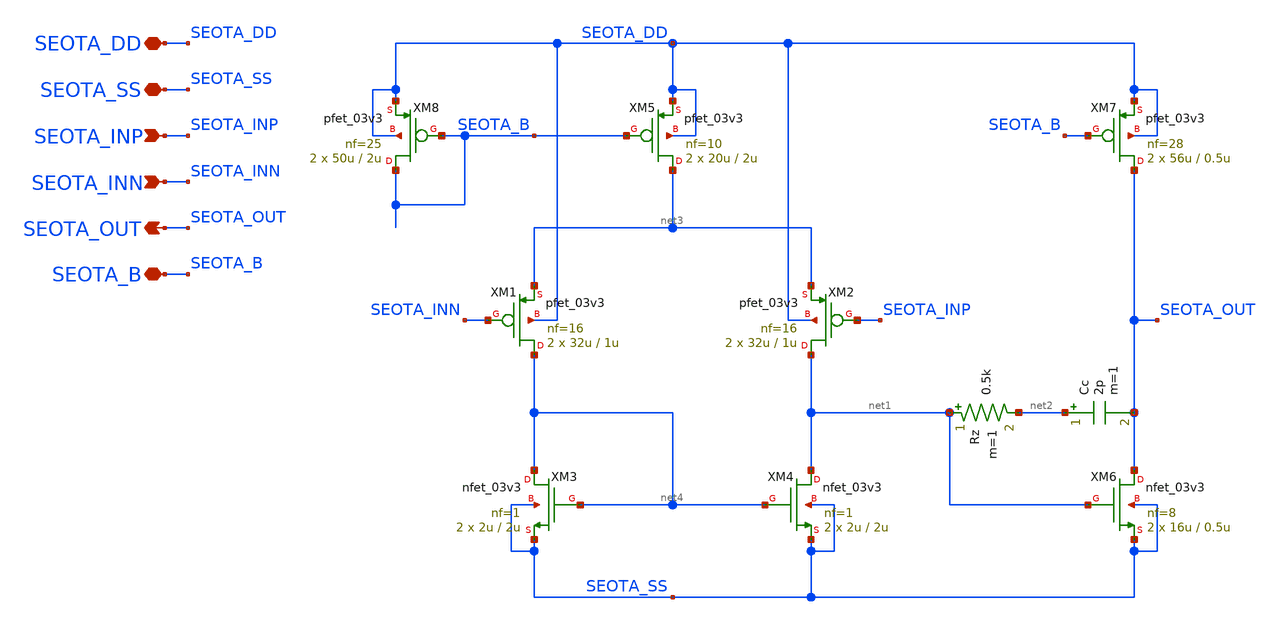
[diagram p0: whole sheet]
** sch_path: Design_Files/IC Design/Schematic/SE_OTA/SE_OTA.sch
**.subckt SE_OTA SEOTA_DD SEOTA_SS SEOTA_INP SEOTA_INN SEOTA_OUT SEOTA_B
*.iopin SEOTA_DD
*.iopin SEOTA_SS
*.ipin SEOTA_INP
*.ipin SEOTA_INN
*.opin SEOTA_OUT
*.iopin SEOTA_B
XM4 net1 net4 SEOTA_SS SEOTA_SS nfet_03v3 L=2u W=2u nf=1 ad='int((nf+1)/2) * W/nf * 0.18u' as='int((nf+2)/2) * W/nf * 0.18u'
+ pd='2*int((nf+1)/2) * (W/nf + 0.18u)' ps='2*int((nf+2)/2) * (W/nf + 0.18u)' nrd='0.18u / W' nrs='0.18u / W'
+ sa=0 sb=0 sd=0 m=2
XM3 net4 net4 SEOTA_SS SEOTA_SS nfet_03v3 L=2u W=2u nf=1 ad='int((nf+1)/2) * W/nf * 0.18u' as='int((nf+2)/2) * W/nf * 0.18u'
+ pd='2*int((nf+1)/2) * (W/nf + 0.18u)' ps='2*int((nf+2)/2) * (W/nf + 0.18u)' nrd='0.18u / W' nrs='0.18u / W'
+ sa=0 sb=0 sd=0 m=2
XM1 net4 SEOTA_INN net3 SEOTA_DD pfet_03v3 L=1u W=32u nf=16 ad='int((nf+1)/2) * W/nf * 0.18u' as='int((nf+2)/2) * W/nf * 0.18u'
+ pd='2*int((nf+1)/2) * (W/nf + 0.18u)' ps='2*int((nf+2)/2) * (W/nf + 0.18u)' nrd='0.18u / W' nrs='0.18u / W'
+ sa=0 sb=0 sd=0 m=2
XM2 net1 SEOTA_INP net3 SEOTA_DD pfet_03v3 L=1u W=32u nf=16 ad='int((nf+1)/2) * W/nf * 0.18u' as='int((nf+2)/2) * W/nf * 0.18u'
+ pd='2*int((nf+1)/2) * (W/nf + 0.18u)' ps='2*int((nf+2)/2) * (W/nf + 0.18u)' nrd='0.18u / W' nrs='0.18u / W'
+ sa=0 sb=0 sd=0 m=2
XM7 SEOTA_OUT SEOTA_B SEOTA_DD SEOTA_DD pfet_03v3 L=0.5u W=56u nf=28 ad='int((nf+1)/2) * W/nf * 0.18u'
+ as='int((nf+2)/2) * W/nf * 0.18u' pd='2*int((nf+1)/2) * (W/nf + 0.18u)' ps='2*int((nf+2)/2) * (W/nf + 0.18u)'
+ nrd='0.18u / W' nrs='0.18u / W' sa=0 sb=0 sd=0 m=2
Rz net1 net2 0.5k m=1
XM5 net3 SEOTA_B SEOTA_DD SEOTA_DD pfet_03v3 L=2u W=20u nf=10 ad='int((nf+1)/2) * W/nf * 0.18u' as='int((nf+2)/2) * W/nf * 0.18u'
+ pd='2*int((nf+1)/2) * (W/nf + 0.18u)' ps='2*int((nf+2)/2) * (W/nf + 0.18u)' nrd='0.18u / W' nrs='0.18u / W'
+ sa=0 sb=0 sd=0 m=2
XM6 SEOTA_OUT net1 SEOTA_SS SEOTA_SS nfet_03v3 L=0.5u W=16u nf=8 ad='int((nf+1)/2) * W/nf * 0.18u' as='int((nf+2)/2) * W/nf * 0.18u'
+ pd='2*int((nf+1)/2) * (W/nf + 0.18u)' ps='2*int((nf+2)/2) * (W/nf + 0.18u)' nrd='0.18u / W' nrs='0.18u / W'
+ sa=0 sb=0 sd=0 m=2
XM8 SEOTA_B SEOTA_B SEOTA_DD SEOTA_DD pfet_03v3 L=2u W=50u nf=25 ad='int((nf+1)/2) * W/nf * 0.18u' as='int((nf+2)/2) * W/nf * 0.18u'
+ pd='2*int((nf+1)/2) * (W/nf + 0.18u)' ps='2*int((nf+2)/2) * (W/nf + 0.18u)' nrd='0.18u / W' nrs='0.18u / W'
+ sa=0 sb=0 sd=0 m=2
Cc net2 SEOTA_OUT 2p m=1
**.ends
.end
